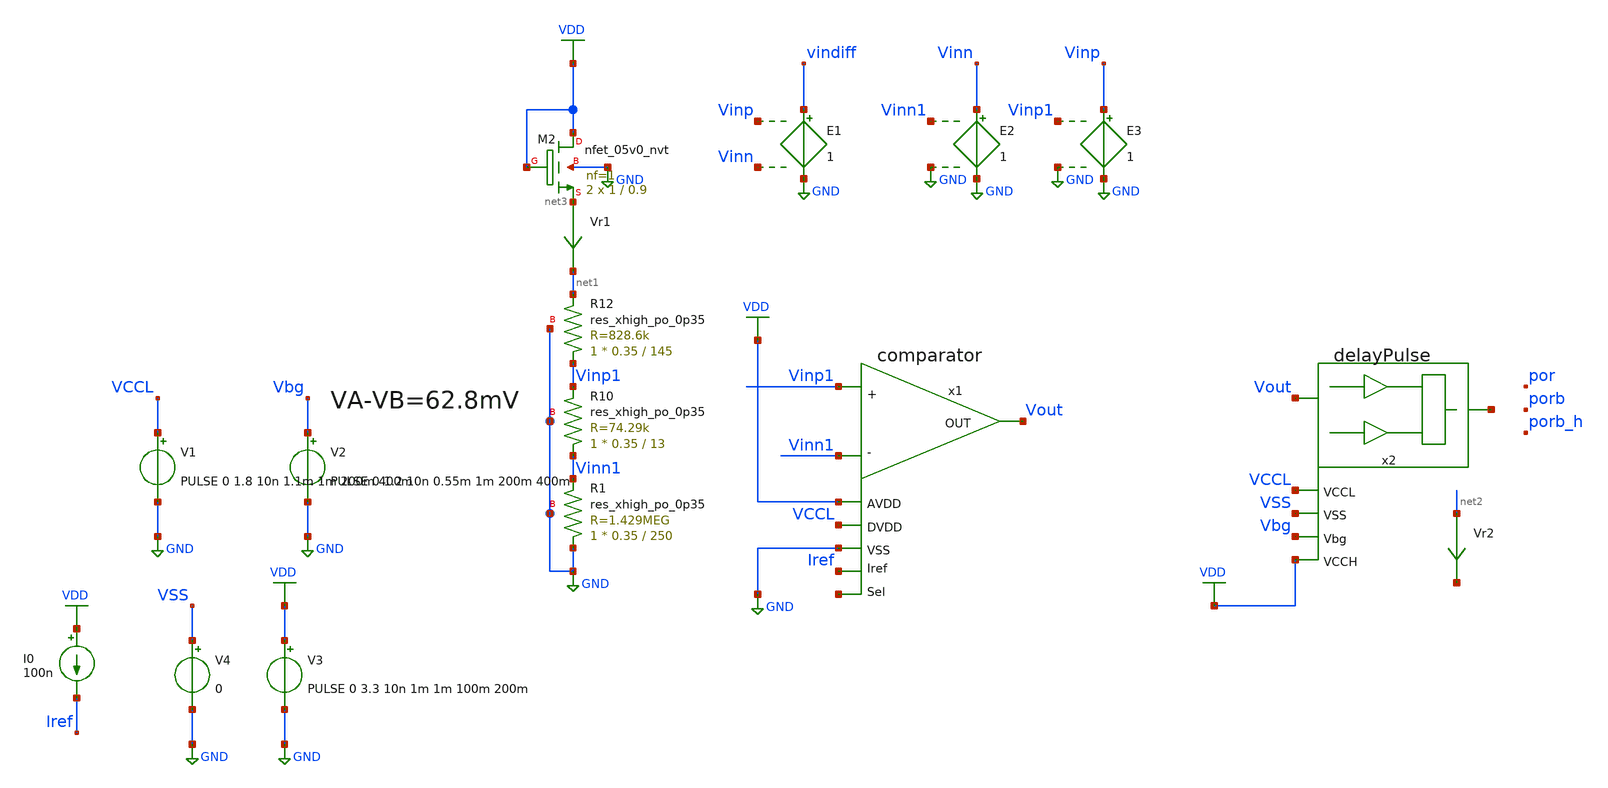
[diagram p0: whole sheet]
** sch_path: xschem_sim/top_por_v2.sch
**.subckt top_por_v2
V3 VDD GND PULSE 0 3.3 10n 1m 1m 100m 200m
I0 VDD Iref 100n
Vr1 net3 net1 0
.save i(vr1)
E1 vindiff GND Vinp Vinn 1
x1 Iref Vinn1 Vinp1 Vout GND VDD VCCL net4 comparator
XR1 GND Vinn1 GND sky130_fd_pr__res_xhigh_po_0p35 L=250 mult=1 m=1
XR10 Vinn1 Vinp1 GND sky130_fd_pr__res_xhigh_po_0p35 L=13 mult=1 m=1
XR12 Vinp1 net1 GND sky130_fd_pr__res_xhigh_po_0p35 L=145 mult=1 m=1
x2 Vout net5 VCCL VSS Vbg VDD delayPulse
V1 VCCL GND PULSE 0 1.8 10n 1.1m 1m 200m 400m
V2 Vbg GND PULSE 0 1.2 10n 0.55m 1m 200m 400m
V4 VSS GND 0
E2 Vinn GND Vinn1 GND 1
E3 Vinp GND Vinp1 GND 1
Vr2 net2 net6 0
.save i(vr2)
XM2 VDD VDD net3 GND sky130_fd_pr__nfet_05v0_nvt L=0.9 W=1 nf=1 ad='int((nf+1)/2) * W/nf * 0.29' as='int((nf+2)/2) * W/nf * 0.29'
+ pd='2*int((nf+1)/2) * (W/nf + 0.29)' ps='2*int((nf+2)/2) * (W/nf + 0.29)' nrd='0.29 / W' nrs='0.29 / W'
+ sa=0 sb=0 sd=0 mult=2 m=2
**** begin user architecture code



* ngspice commands
*.param W=1
.options savecurrents
*.dc v3 0 3.3 0.01
.control
  set temp=-40
  save all
  save @m.xm1.msky130_fd_pr__nfet_05v0_nvt[gm]
  save @m.xm1.msky130_fd_pr__nfet_05v0_nvt[id]
  op
  write top_por_v2.raw
  set appendwrite
  *dc v3 0 3.3 0.01
  tran .5u 2m
  *tran 1u 55m
  meas tran Ivdd AVG i(V3)
  meas tran yAvdd FIND v(vdd) WHEN v(por)=0.9 RISE=1
  meas tran porPulse TRIG v(por) VAL=0.9 RISE=1 TARG v(por) VAL=0.9 FALL=1
  write top_por_v2.raw
  *quit 0

.endc



 .lib $::SKYWATER_MODELS/sky130.lib.spice tt

.include $::SKYWATER_STDCELLS/sky130_fd_sc_hd.spice
.include $::SKYWATER_STDCELLS/../../sky130_fd_sc_hvl/spice/sky130_fd_sc_hvl.spice


**** end user architecture code
**.ends
.GLOBAL GND
.GLOBAL VDD
.end
